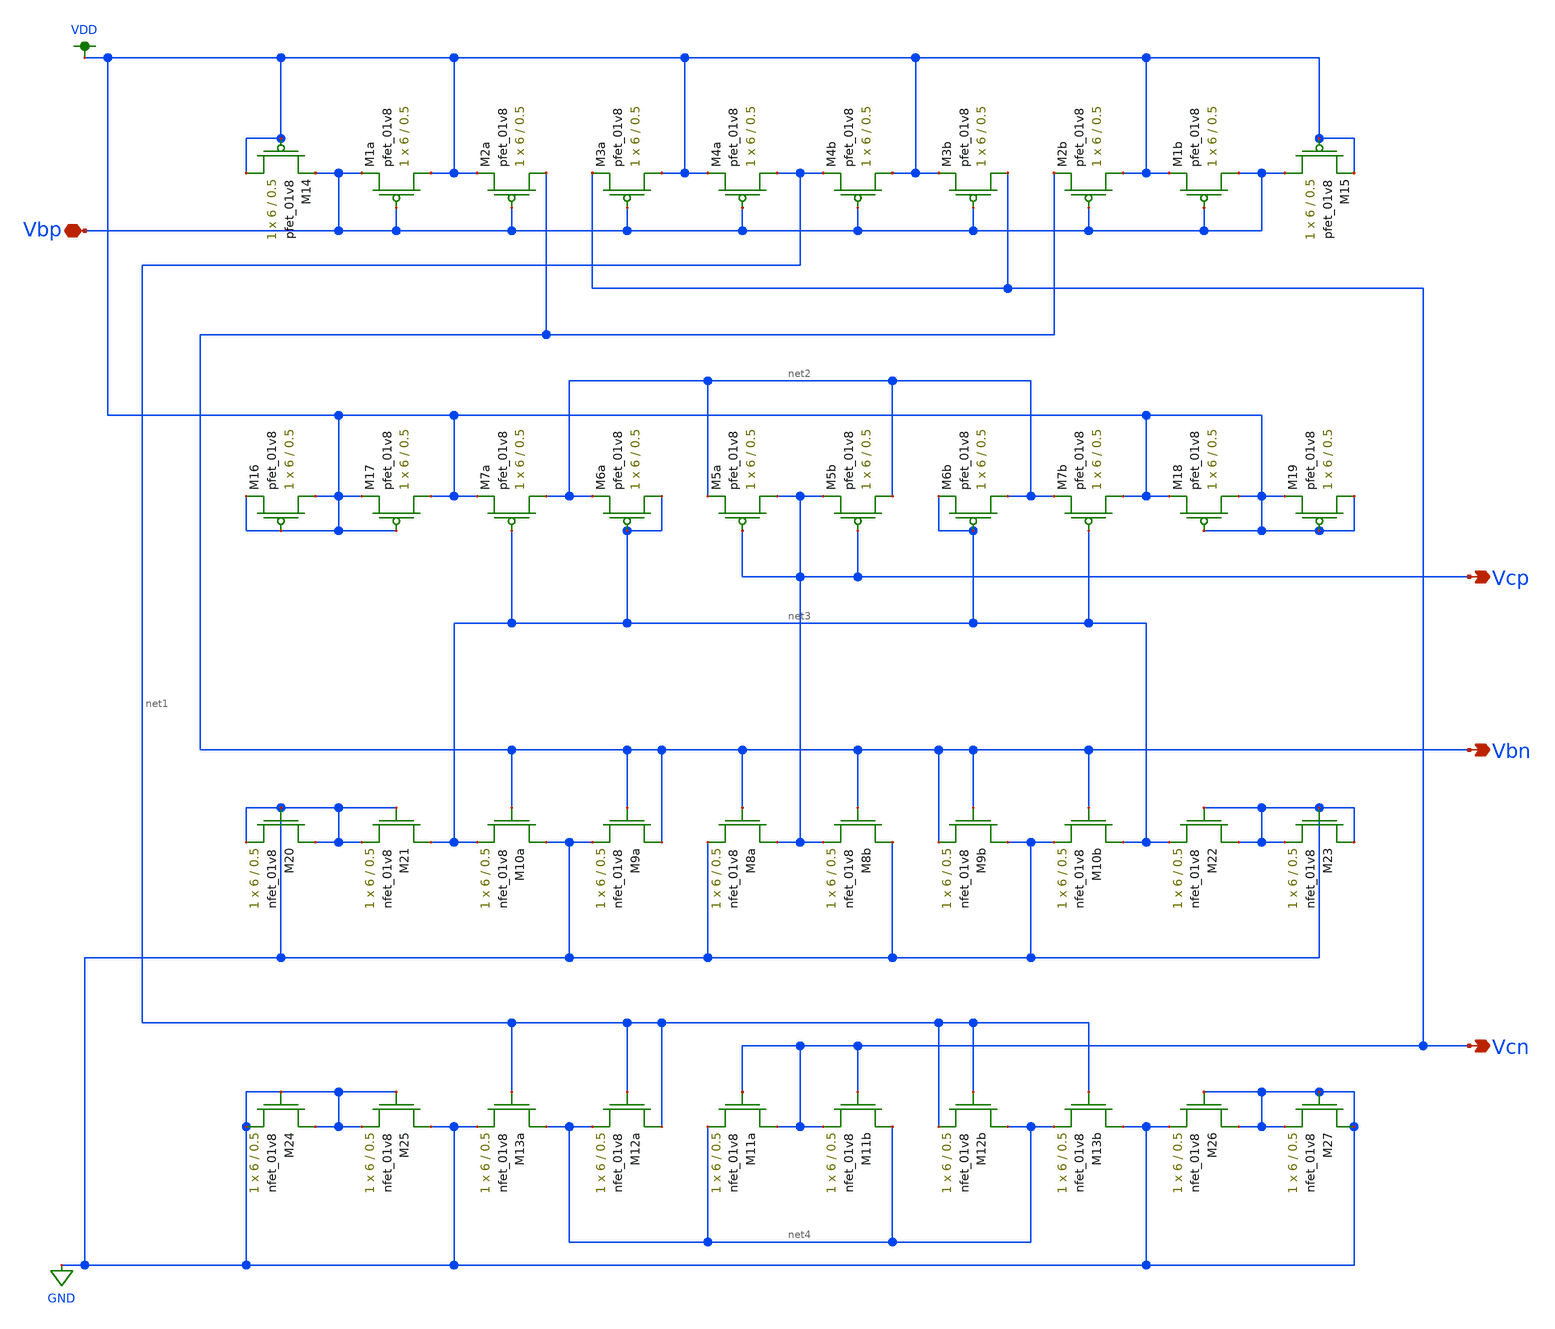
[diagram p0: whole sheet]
** sch_path: schematic/lvs_schematic/cascode_bias_xschem.sch
**.subckt cascode_bias_xschem Vcp Vbn Vcn Vbp
*.opin Vcp
*.opin Vbn
*.opin Vcn
*.iopin Vbp
XM1a VDD Vbp Vbp VDD sky130_fd_pr__pfet_01v8 L=0.5 W=6 nf=1 ad='int((nf+1)/2) * W/nf * 0.29' as='int((nf+2)/2) * W/nf * 0.29'
+ pd='2*int((nf+1)/2) * (W/nf + 0.29)' ps='2*int((nf+2)/2) * (W/nf + 0.29)' nrd='0.29 / W' nrs='0.29 / W'
+ sa=0 sb=0 sd=0 mult=1 m=1
XM2a Vbn Vbp VDD VDD sky130_fd_pr__pfet_01v8 L=0.5 W=6 nf=1 ad='int((nf+1)/2) * W/nf * 0.29' as='int((nf+2)/2) * W/nf * 0.29'
+ pd='2*int((nf+1)/2) * (W/nf + 0.29)' ps='2*int((nf+2)/2) * (W/nf + 0.29)' nrd='0.29 / W' nrs='0.29 / W'
+ sa=0 sb=0 sd=0 mult=1 m=1
XM3a VDD Vbp Vcn VDD sky130_fd_pr__pfet_01v8 L=0.5 W=6 nf=1 ad='int((nf+1)/2) * W/nf * 0.29' as='int((nf+2)/2) * W/nf * 0.29'
+ pd='2*int((nf+1)/2) * (W/nf + 0.29)' ps='2*int((nf+2)/2) * (W/nf + 0.29)' nrd='0.29 / W' nrs='0.29 / W'
+ sa=0 sb=0 sd=0 mult=1 m=1
XM4a net1 Vbp VDD VDD sky130_fd_pr__pfet_01v8 L=0.5 W=6 nf=1 ad='int((nf+1)/2) * W/nf * 0.29' as='int((nf+2)/2) * W/nf * 0.29'
+ pd='2*int((nf+1)/2) * (W/nf + 0.29)' ps='2*int((nf+2)/2) * (W/nf + 0.29)' nrd='0.29 / W' nrs='0.29 / W'
+ sa=0 sb=0 sd=0 mult=1 m=1
XM4b VDD Vbp net1 VDD sky130_fd_pr__pfet_01v8 L=0.5 W=6 nf=1 ad='int((nf+1)/2) * W/nf * 0.29' as='int((nf+2)/2) * W/nf * 0.29'
+ pd='2*int((nf+1)/2) * (W/nf + 0.29)' ps='2*int((nf+2)/2) * (W/nf + 0.29)' nrd='0.29 / W' nrs='0.29 / W'
+ sa=0 sb=0 sd=0 mult=1 m=1
XM3b Vcn Vbp VDD VDD sky130_fd_pr__pfet_01v8 L=0.5 W=6 nf=1 ad='int((nf+1)/2) * W/nf * 0.29' as='int((nf+2)/2) * W/nf * 0.29'
+ pd='2*int((nf+1)/2) * (W/nf + 0.29)' ps='2*int((nf+2)/2) * (W/nf + 0.29)' nrd='0.29 / W' nrs='0.29 / W'
+ sa=0 sb=0 sd=0 mult=1 m=1
XM2b VDD Vbp Vbn VDD sky130_fd_pr__pfet_01v8 L=0.5 W=6 nf=1 ad='int((nf+1)/2) * W/nf * 0.29' as='int((nf+2)/2) * W/nf * 0.29'
+ pd='2*int((nf+1)/2) * (W/nf + 0.29)' ps='2*int((nf+2)/2) * (W/nf + 0.29)' nrd='0.29 / W' nrs='0.29 / W'
+ sa=0 sb=0 sd=0 mult=1 m=1
XM1b Vbp Vbp VDD VDD sky130_fd_pr__pfet_01v8 L=0.5 W=6 nf=1 ad='int((nf+1)/2) * W/nf * 0.29' as='int((nf+2)/2) * W/nf * 0.29'
+ pd='2*int((nf+1)/2) * (W/nf + 0.29)' ps='2*int((nf+2)/2) * (W/nf + 0.29)' nrd='0.29 / W' nrs='0.29 / W'
+ sa=0 sb=0 sd=0 mult=1 m=1
XM7a net2 net3 VDD VDD sky130_fd_pr__pfet_01v8 L=0.5 W=6 nf=1 ad='int((nf+1)/2) * W/nf * 0.29' as='int((nf+2)/2) * W/nf * 0.29'
+ pd='2*int((nf+1)/2) * (W/nf + 0.29)' ps='2*int((nf+2)/2) * (W/nf + 0.29)' nrd='0.29 / W' nrs='0.29 / W'
+ sa=0 sb=0 sd=0 mult=1 m=1
XM6a net3 net3 net2 VDD sky130_fd_pr__pfet_01v8 L=0.5 W=6 nf=1 ad='int((nf+1)/2) * W/nf * 0.29' as='int((nf+2)/2) * W/nf * 0.29'
+ pd='2*int((nf+1)/2) * (W/nf + 0.29)' ps='2*int((nf+2)/2) * (W/nf + 0.29)' nrd='0.29 / W' nrs='0.29 / W'
+ sa=0 sb=0 sd=0 mult=1 m=1
XM5a Vcp Vcp net2 VDD sky130_fd_pr__pfet_01v8 L=0.5 W=6 nf=1 ad='int((nf+1)/2) * W/nf * 0.29' as='int((nf+2)/2) * W/nf * 0.29'
+ pd='2*int((nf+1)/2) * (W/nf + 0.29)' ps='2*int((nf+2)/2) * (W/nf + 0.29)' nrd='0.29 / W' nrs='0.29 / W'
+ sa=0 sb=0 sd=0 mult=1 m=1
XM5b net2 Vcp Vcp VDD sky130_fd_pr__pfet_01v8 L=0.5 W=6 nf=1 ad='int((nf+1)/2) * W/nf * 0.29' as='int((nf+2)/2) * W/nf * 0.29'
+ pd='2*int((nf+1)/2) * (W/nf + 0.29)' ps='2*int((nf+2)/2) * (W/nf + 0.29)' nrd='0.29 / W' nrs='0.29 / W'
+ sa=0 sb=0 sd=0 mult=1 m=1
XM6b net2 net3 net3 VDD sky130_fd_pr__pfet_01v8 L=0.5 W=6 nf=1 ad='int((nf+1)/2) * W/nf * 0.29' as='int((nf+2)/2) * W/nf * 0.29'
+ pd='2*int((nf+1)/2) * (W/nf + 0.29)' ps='2*int((nf+2)/2) * (W/nf + 0.29)' nrd='0.29 / W' nrs='0.29 / W'
+ sa=0 sb=0 sd=0 mult=1 m=1
XM7b VDD net3 net2 VDD sky130_fd_pr__pfet_01v8 L=0.5 W=6 nf=1 ad='int((nf+1)/2) * W/nf * 0.29' as='int((nf+2)/2) * W/nf * 0.29'
+ pd='2*int((nf+1)/2) * (W/nf + 0.29)' ps='2*int((nf+2)/2) * (W/nf + 0.29)' nrd='0.29 / W' nrs='0.29 / W'
+ sa=0 sb=0 sd=0 mult=1 m=1
XM8a Vcp Vbn GND GND sky130_fd_pr__nfet_01v8 L=0.5 W=6 nf=1 ad='int((nf+1)/2) * W/nf * 0.29' as='int((nf+2)/2) * W/nf * 0.29'
+ pd='2*int((nf+1)/2) * (W/nf + 0.29)' ps='2*int((nf+2)/2) * (W/nf + 0.29)' nrd='0.29 / W' nrs='0.29 / W'
+ sa=0 sb=0 sd=0 mult=1 m=1
XM8b GND Vbn Vcp GND sky130_fd_pr__nfet_01v8 L=0.5 W=6 nf=1 ad='int((nf+1)/2) * W/nf * 0.29' as='int((nf+2)/2) * W/nf * 0.29'
+ pd='2*int((nf+1)/2) * (W/nf + 0.29)' ps='2*int((nf+2)/2) * (W/nf + 0.29)' nrd='0.29 / W' nrs='0.29 / W'
+ sa=0 sb=0 sd=0 mult=1 m=1
XM10a GND Vbn net3 GND sky130_fd_pr__nfet_01v8 L=0.5 W=6 nf=1 ad='int((nf+1)/2) * W/nf * 0.29' as='int((nf+2)/2) * W/nf * 0.29'
+ pd='2*int((nf+1)/2) * (W/nf + 0.29)' ps='2*int((nf+2)/2) * (W/nf + 0.29)' nrd='0.29 / W' nrs='0.29 / W'
+ sa=0 sb=0 sd=0 mult=1 m=1
XM9a Vbn Vbn GND GND sky130_fd_pr__nfet_01v8 L=0.5 W=6 nf=1 ad='int((nf+1)/2) * W/nf * 0.29' as='int((nf+2)/2) * W/nf * 0.29'
+ pd='2*int((nf+1)/2) * (W/nf + 0.29)' ps='2*int((nf+2)/2) * (W/nf + 0.29)' nrd='0.29 / W' nrs='0.29 / W'
+ sa=0 sb=0 sd=0 mult=1 m=1
XM9b GND Vbn Vbn GND sky130_fd_pr__nfet_01v8 L=0.5 W=6 nf=1 ad='int((nf+1)/2) * W/nf * 0.29' as='int((nf+2)/2) * W/nf * 0.29'
+ pd='2*int((nf+1)/2) * (W/nf + 0.29)' ps='2*int((nf+2)/2) * (W/nf + 0.29)' nrd='0.29 / W' nrs='0.29 / W'
+ sa=0 sb=0 sd=0 mult=1 m=1
XM10b net3 Vbn GND GND sky130_fd_pr__nfet_01v8 L=0.5 W=6 nf=1 ad='int((nf+1)/2) * W/nf * 0.29' as='int((nf+2)/2) * W/nf * 0.29'
+ pd='2*int((nf+1)/2) * (W/nf + 0.29)' ps='2*int((nf+2)/2) * (W/nf + 0.29)' nrd='0.29 / W' nrs='0.29 / W'
+ sa=0 sb=0 sd=0 mult=1 m=1
XM11a Vcn Vcn net4 GND sky130_fd_pr__nfet_01v8 L=0.5 W=6 nf=1 ad='int((nf+1)/2) * W/nf * 0.29' as='int((nf+2)/2) * W/nf * 0.29'
+ pd='2*int((nf+1)/2) * (W/nf + 0.29)' ps='2*int((nf+2)/2) * (W/nf + 0.29)' nrd='0.29 / W' nrs='0.29 / W'
+ sa=0 sb=0 sd=0 mult=1 m=1
XM11b net4 Vcn Vcn GND sky130_fd_pr__nfet_01v8 L=0.5 W=6 nf=1 ad='int((nf+1)/2) * W/nf * 0.29' as='int((nf+2)/2) * W/nf * 0.29'
+ pd='2*int((nf+1)/2) * (W/nf + 0.29)' ps='2*int((nf+2)/2) * (W/nf + 0.29)' nrd='0.29 / W' nrs='0.29 / W'
+ sa=0 sb=0 sd=0 mult=1 m=1
XM13a net4 net1 GND GND sky130_fd_pr__nfet_01v8 L=0.5 W=6 nf=1 ad='int((nf+1)/2) * W/nf * 0.29' as='int((nf+2)/2) * W/nf * 0.29'
+ pd='2*int((nf+1)/2) * (W/nf + 0.29)' ps='2*int((nf+2)/2) * (W/nf + 0.29)' nrd='0.29 / W' nrs='0.29 / W'
+ sa=0 sb=0 sd=0 mult=1 m=1
XM12a net1 net1 net4 GND sky130_fd_pr__nfet_01v8 L=0.5 W=6 nf=1 ad='int((nf+1)/2) * W/nf * 0.29' as='int((nf+2)/2) * W/nf * 0.29'
+ pd='2*int((nf+1)/2) * (W/nf + 0.29)' ps='2*int((nf+2)/2) * (W/nf + 0.29)' nrd='0.29 / W' nrs='0.29 / W'
+ sa=0 sb=0 sd=0 mult=1 m=1
XM12b net4 net1 net1 GND sky130_fd_pr__nfet_01v8 L=0.5 W=6 nf=1 ad='int((nf+1)/2) * W/nf * 0.29' as='int((nf+2)/2) * W/nf * 0.29'
+ pd='2*int((nf+1)/2) * (W/nf + 0.29)' ps='2*int((nf+2)/2) * (W/nf + 0.29)' nrd='0.29 / W' nrs='0.29 / W'
+ sa=0 sb=0 sd=0 mult=1 m=1
XM13b GND net1 net4 GND sky130_fd_pr__nfet_01v8 L=0.5 W=6 nf=1 ad='int((nf+1)/2) * W/nf * 0.29' as='int((nf+2)/2) * W/nf * 0.29'
+ pd='2*int((nf+1)/2) * (W/nf + 0.29)' ps='2*int((nf+2)/2) * (W/nf + 0.29)' nrd='0.29 / W' nrs='0.29 / W'
+ sa=0 sb=0 sd=0 mult=1 m=1
XM15 Vbp VDD VDD VDD sky130_fd_pr__pfet_01v8 L=0.5 W=6 nf=1 ad='int((nf+1)/2) * W/nf * 0.29' as='int((nf+2)/2) * W/nf * 0.29'
+ pd='2*int((nf+1)/2) * (W/nf + 0.29)' ps='2*int((nf+2)/2) * (W/nf + 0.29)' nrd='0.29 / W' nrs='0.29 / W'
+ sa=0 sb=0 sd=0 mult=1 m=1
XM25 GND GND GND GND sky130_fd_pr__nfet_01v8 L=0.5 W=6 nf=1 ad='int((nf+1)/2) * W/nf * 0.29' as='int((nf+2)/2) * W/nf * 0.29'
+ pd='2*int((nf+1)/2) * (W/nf + 0.29)' ps='2*int((nf+2)/2) * (W/nf + 0.29)' nrd='0.29 / W' nrs='0.29 / W'
+ sa=0 sb=0 sd=0 mult=1 m=1
XM24 GND GND GND GND sky130_fd_pr__nfet_01v8 L=0.5 W=6 nf=1 ad='int((nf+1)/2) * W/nf * 0.29' as='int((nf+2)/2) * W/nf * 0.29'
+ pd='2*int((nf+1)/2) * (W/nf + 0.29)' ps='2*int((nf+2)/2) * (W/nf + 0.29)' nrd='0.29 / W' nrs='0.29 / W'
+ sa=0 sb=0 sd=0 mult=1 m=1
XM26 GND GND GND GND sky130_fd_pr__nfet_01v8 L=0.5 W=6 nf=1 ad='int((nf+1)/2) * W/nf * 0.29' as='int((nf+2)/2) * W/nf * 0.29'
+ pd='2*int((nf+1)/2) * (W/nf + 0.29)' ps='2*int((nf+2)/2) * (W/nf + 0.29)' nrd='0.29 / W' nrs='0.29 / W'
+ sa=0 sb=0 sd=0 mult=1 m=1
XM27 GND GND GND GND sky130_fd_pr__nfet_01v8 L=0.5 W=6 nf=1 ad='int((nf+1)/2) * W/nf * 0.29' as='int((nf+2)/2) * W/nf * 0.29'
+ pd='2*int((nf+1)/2) * (W/nf + 0.29)' ps='2*int((nf+2)/2) * (W/nf + 0.29)' nrd='0.29 / W' nrs='0.29 / W'
+ sa=0 sb=0 sd=0 mult=1 m=1
XM21 net3 GND GND GND sky130_fd_pr__nfet_01v8 L=0.5 W=6 nf=1 ad='int((nf+1)/2) * W/nf * 0.29' as='int((nf+2)/2) * W/nf * 0.29'
+ pd='2*int((nf+1)/2) * (W/nf + 0.29)' ps='2*int((nf+2)/2) * (W/nf + 0.29)' nrd='0.29 / W' nrs='0.29 / W'
+ sa=0 sb=0 sd=0 mult=1 m=1
XM20 GND GND GND GND sky130_fd_pr__nfet_01v8 L=0.5 W=6 nf=1 ad='int((nf+1)/2) * W/nf * 0.29' as='int((nf+2)/2) * W/nf * 0.29'
+ pd='2*int((nf+1)/2) * (W/nf + 0.29)' ps='2*int((nf+2)/2) * (W/nf + 0.29)' nrd='0.29 / W' nrs='0.29 / W'
+ sa=0 sb=0 sd=0 mult=1 m=1
XM23 GND GND GND GND sky130_fd_pr__nfet_01v8 L=0.5 W=6 nf=1 ad='int((nf+1)/2) * W/nf * 0.29' as='int((nf+2)/2) * W/nf * 0.29'
+ pd='2*int((nf+1)/2) * (W/nf + 0.29)' ps='2*int((nf+2)/2) * (W/nf + 0.29)' nrd='0.29 / W' nrs='0.29 / W'
+ sa=0 sb=0 sd=0 mult=1 m=1
XM22 GND GND net3 GND sky130_fd_pr__nfet_01v8 L=0.5 W=6 nf=1 ad='int((nf+1)/2) * W/nf * 0.29' as='int((nf+2)/2) * W/nf * 0.29'
+ pd='2*int((nf+1)/2) * (W/nf + 0.29)' ps='2*int((nf+2)/2) * (W/nf + 0.29)' nrd='0.29 / W' nrs='0.29 / W'
+ sa=0 sb=0 sd=0 mult=1 m=1
XM14 VDD VDD Vbp VDD sky130_fd_pr__pfet_01v8 L=0.5 W=6 nf=1 ad='int((nf+1)/2) * W/nf * 0.29' as='int((nf+2)/2) * W/nf * 0.29'
+ pd='2*int((nf+1)/2) * (W/nf + 0.29)' ps='2*int((nf+2)/2) * (W/nf + 0.29)' nrd='0.29 / W' nrs='0.29 / W'
+ sa=0 sb=0 sd=0 mult=1 m=1
XM17 VDD VDD VDD VDD sky130_fd_pr__pfet_01v8 L=0.5 W=6 nf=1 ad='int((nf+1)/2) * W/nf * 0.29' as='int((nf+2)/2) * W/nf * 0.29'
+ pd='2*int((nf+1)/2) * (W/nf + 0.29)' ps='2*int((nf+2)/2) * (W/nf + 0.29)' nrd='0.29 / W' nrs='0.29 / W'
+ sa=0 sb=0 sd=0 mult=1 m=1
XM16 VDD VDD VDD VDD sky130_fd_pr__pfet_01v8 L=0.5 W=6 nf=1 ad='int((nf+1)/2) * W/nf * 0.29' as='int((nf+2)/2) * W/nf * 0.29'
+ pd='2*int((nf+1)/2) * (W/nf + 0.29)' ps='2*int((nf+2)/2) * (W/nf + 0.29)' nrd='0.29 / W' nrs='0.29 / W'
+ sa=0 sb=0 sd=0 mult=1 m=1
XM18 VDD VDD VDD VDD sky130_fd_pr__pfet_01v8 L=0.5 W=6 nf=1 ad='int((nf+1)/2) * W/nf * 0.29' as='int((nf+2)/2) * W/nf * 0.29'
+ pd='2*int((nf+1)/2) * (W/nf + 0.29)' ps='2*int((nf+2)/2) * (W/nf + 0.29)' nrd='0.29 / W' nrs='0.29 / W'
+ sa=0 sb=0 sd=0 mult=1 m=1
XM19 VDD VDD VDD VDD sky130_fd_pr__pfet_01v8 L=0.5 W=6 nf=1 ad='int((nf+1)/2) * W/nf * 0.29' as='int((nf+2)/2) * W/nf * 0.29'
+ pd='2*int((nf+1)/2) * (W/nf + 0.29)' ps='2*int((nf+2)/2) * (W/nf + 0.29)' nrd='0.29 / W' nrs='0.29 / W'
+ sa=0 sb=0 sd=0 mult=1 m=1
**.ends
.GLOBAL VDD
.GLOBAL GND
.end
